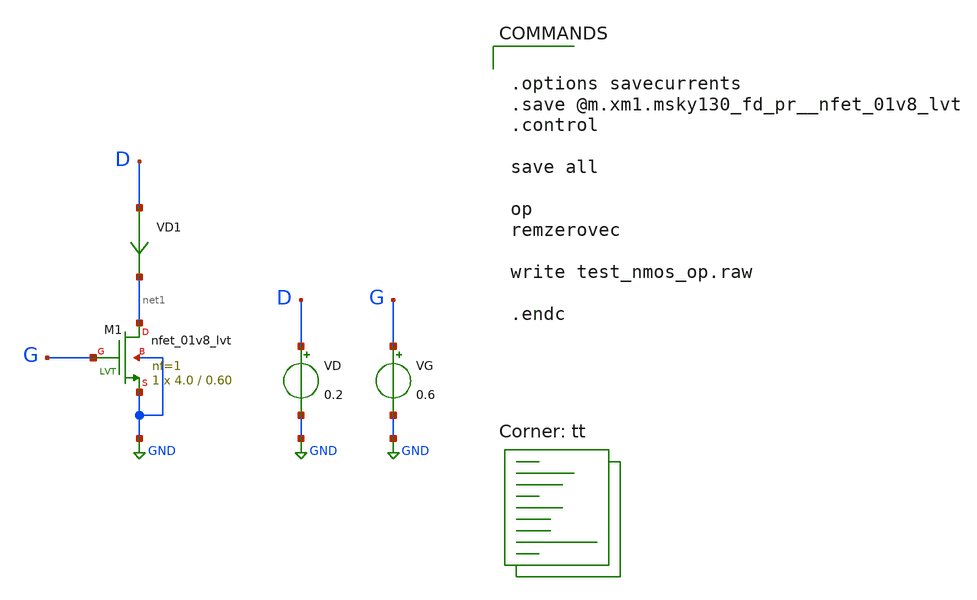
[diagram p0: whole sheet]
** sch_path: strongARM/test_nmos_op.sch
**.subckt test_nmos_op
VG G GND 0.6
VD D GND 0.2
VD1 D net1 0
.save i(vd1)
XM1 net1 G GND GND sky130_fd_pr__nfet_01v8_lvt L=0.60 W=4.0 nf=1 ad='int((nf+1)/2) * W/nf * 0.29' as='int((nf+2)/2) * W/nf * 0.29'
+ pd='2*int((nf+1)/2) * (W/nf + 0.29)' ps='2*int((nf+2)/2) * (W/nf + 0.29)' nrd='0.29 / W' nrs='0.29 / W'
+ sa=0 sb=0 sd=0 mult=1 m=1
**** begin user architecture code
.lib $::SKYWATER_MODELS/sky130.lib.spice tt


.options savecurrents
.save @m.xm1.msky130_fd_pr__nfet_01v8_lvt
.control

save all

op
remzerovec

write test_nmos_op.raw

.endc


**** end user architecture code
**.ends
.GLOBAL GND
.end
